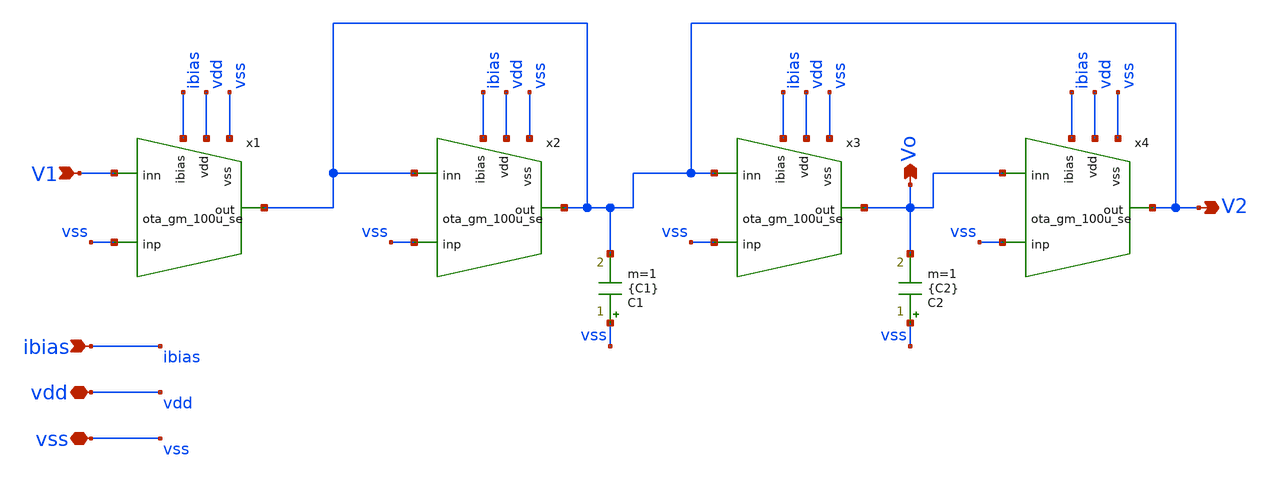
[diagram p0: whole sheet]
** sch_path: prj/template/3_Real_circuits/biquad_gm_c_se.sch
* prj/template/3_Real_circuits/ota_gm_100u_se.sch:
* (c) 2024-2025 M. Meiners, Apache-2.0 license
**.subckt biquad_gm_c_se V1 Vo V2 ibias vdd vss
*.ipin V1
*.opin Vo
*.opin V2
*.ipin ibias
*.iopin vdd
*.iopin vss
C1 vss V2 {C1} m=1
C2 vss Vo {C2} m=1
x1 vss V1 V2 ibias vdd vss ota_gm_100u_se
x2 vss V2 V2 ibias vdd vss ota_gm_100u_se
x3 vss V2 Vo ibias vdd vss ota_gm_100u_se
x4 vss Vo V2 ibias vdd vss ota_gm_100u_se
**.ends

* expanding   symbol:  ota_gm_100u_se.sym # of pins=8
** sym_path: prj/template/3_Real_circuits/ota_gm_100u_se.sym
** sch_path: prj/template/3_Real_circuits/ota_gm_100u_se.sch
.subckt ota_gm_100u_se inp inn out ibias vdd vss
*.ipin ibias
*.iopin vdd
*.iopin vss
*.ipin inp
*.ipin inn
*.opin out
XM5 tail ibias vss vss sg13_lv_nmos w=14u l=5u ng=10 m=1 mm_ok=1
XM4 out gate_p vdd vdd sg13_lv_pmos w=31u l=5u ng=10 m=1 mm_ok=1
XM1 gate_p inp tail tail sg13_lv_nmos w=33u l=5u ng=10 m=1 mm_ok=1
XM2 out inn tail tail sg13_lv_nmos w=33u l=5u ng=10 m=1 mm_ok=1
XM3 gate_p gate_p vdd vdd sg13_lv_pmos w=31u l=5u ng=10 m=1 mm_ok=1
XM6 ibias ibias vss vss sg13_lv_nmos w=18u l=5u ng=10 m=1 mm_ok=1
.ends

.end
